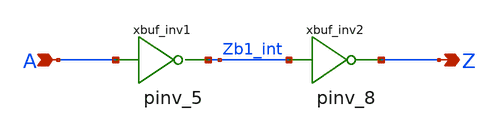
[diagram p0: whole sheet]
** sch_path: sram_2_16_scn4m/pdriver_4.sch
**.subckt pdriver_4 A Z
*.ipin A
*.opin Z
xbuf_inv1 A Zb1_int vdd gnd pinv_5
xbuf_inv2 Zb1_int Z vdd gnd pinv_8
**.ends

* expanding   symbol:  pinv_5.sym # of pins=2
** sym_path: sram_2_16_scn4m/pinv_5.sym
** sch_path: sram_2_16_scn4m/pinv_5.sch
.subckt pinv_5 A Z vdd gnd
*.ipin A
*.opin Z
XMpinv_nmos Z A gnd gnd sky130_fd_pr__nfet_01v8 L=0.4 W=0.8 nf=1 ad='int((nf+1)/2) * W/nf * 0.29' as='int((nf+2)/2) * W/nf * 0.29'
+ pd='2*int((nf+1)/2) * (W/nf + 0.29)' ps='2*int((nf+2)/2) * (W/nf + 0.29)' nrd='0.29 / W' nrs='0.29 / W'
+ sa=0 sb=0 sd=0 mult=1 m=1
XMp_inv_pmos Z A vdd vdd sky130_fd_pr__pfet_01v8 L=0.4 W=1.6 nf=1 ad='int((nf+1)/2) * W/nf * 0.29' as='int((nf+2)/2) * W/nf * 0.29'
+ pd='2*int((nf+1)/2) * (W/nf + 0.29)' ps='2*int((nf+2)/2) * (W/nf + 0.29)' nrd='0.29 / W' nrs='0.29 / W'
+ sa=0 sb=0 sd=0 mult=1 m=1
.ends


* expanding   symbol:  pinv_8.sym # of pins=2
** sym_path: sram_2_64_scn4m/pinv_8.sym
** sch_path: sram_2_64_scn4m/pinv_8.sch
.subckt pinv_8 A Z vdd gnd
*.ipin A
*.opin Z
XMpinv_nmos Z A gnd gnd sky130_fd_pr__nfet_01v8 L=0.4 W=2.8 nf=1 ad='int((nf+1)/2) * W/nf * 0.29' as='int((nf+2)/2) * W/nf * 0.29'
+ pd='2*int((nf+1)/2) * (W/nf + 0.29)' ps='2*int((nf+2)/2) * (W/nf + 0.29)' nrd='0.29 / W' nrs='0.29 / W'
+ sa=0 sb=0 sd=0 mult=1 m=1
XMp_inv_pmos Z A vdd vdd sky130_fd_pr__pfet_01v8 L=0.4 W=5.6 nf=1 ad='int((nf+1)/2) * W/nf * 0.29' as='int((nf+2)/2) * W/nf * 0.29'
+ pd='2*int((nf+1)/2) * (W/nf + 0.29)' ps='2*int((nf+2)/2) * (W/nf + 0.29)' nrd='0.29 / W' nrs='0.29 / W'
+ sa=0 sb=0 sd=0 mult=1 m=1
.ends

.end
